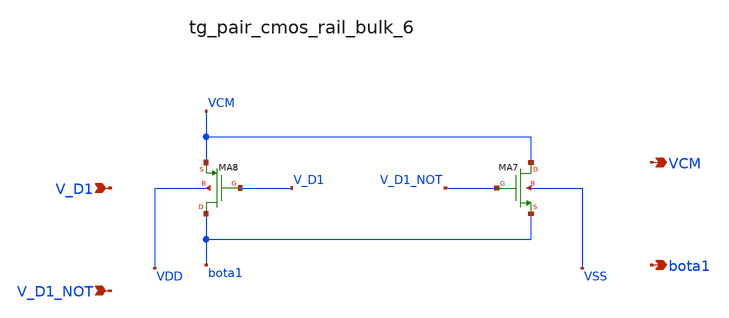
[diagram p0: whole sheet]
** sch_path: analog-db/raw/ia_005_hsu_pga_ideal/hier/blocks/tg_pair_cmos_rail_bulk_6.sch
**.subckt tg_pair_cmos_rail_bulk_6 V_D1 V_D1_NOT VCM bota1
*.ipin V_D1
*.ipin V_D1_NOT
*.opin VCM
*.opin bota1
XMA7 VCM V_D1_NOT bota1 VSS sg13_lv_nmos w=x_dut_xma7_w l=x_dut_xma7_l ng=1 m=x_dut_xma7_m
XMA8 bota1 V_D1 VCM VDD sg13_lv_pmos w=x_dut_xma8_w l=x_dut_xma8_l ng=1 m=x_dut_xma8_m
**.ends
.end
